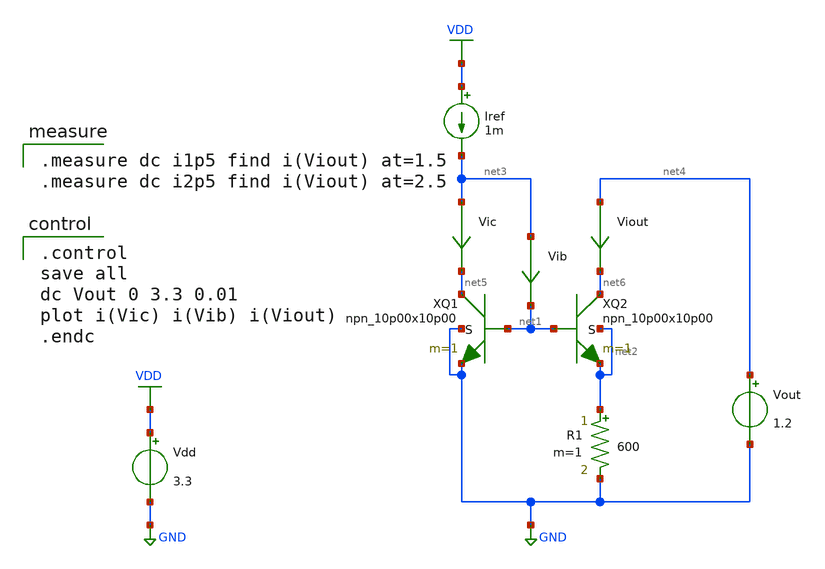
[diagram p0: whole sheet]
** sch_path: current-source/cm-widlar-bjt.sch
**.subckt cm-widlar-bjt
XQ2 net6 net1 net2 net2 npn_10p00x10p00 m=1
XQ1 net5 net1 GND GND npn_10p00x10p00 m=1
Viout net4 net6 0
.save i(viout)
Vdd VDD GND 3.3
Iref VDD net3 1m
Vic net3 net5 0
.save i(vic)
Vib net3 net1 0
.save i(vib)
Vout net4 GND 1.2
R1 net2 GND 600 m=1
**** begin user architecture code

.include $::180MCU_MODELS/design.ngspice
.lib $::180MCU_MODELS/sm141064.ngspice typical
.lib $::180MCU_MODELS/sm141064.ngspice res_typical
.lib $::180MCU_MODELS/sm141064.ngspice moscap_typical
.lib $::180MCU_MODELS/sm141064.ngspice bjt_typical
* .lib $::180MCU_MODELS/sm141064.ngspice res_statistical


.control
save all
dc Vout 0 3.3 0.01
plot i(Vic) i(Vib) i(Viout)
.endc


.measure dc i1p5 find i(Viout) at=1.5
.measure dc i2p5 find i(Viout) at=2.5

**** end user architecture code
**.ends
.GLOBAL GND
.GLOBAL VDD
.end
